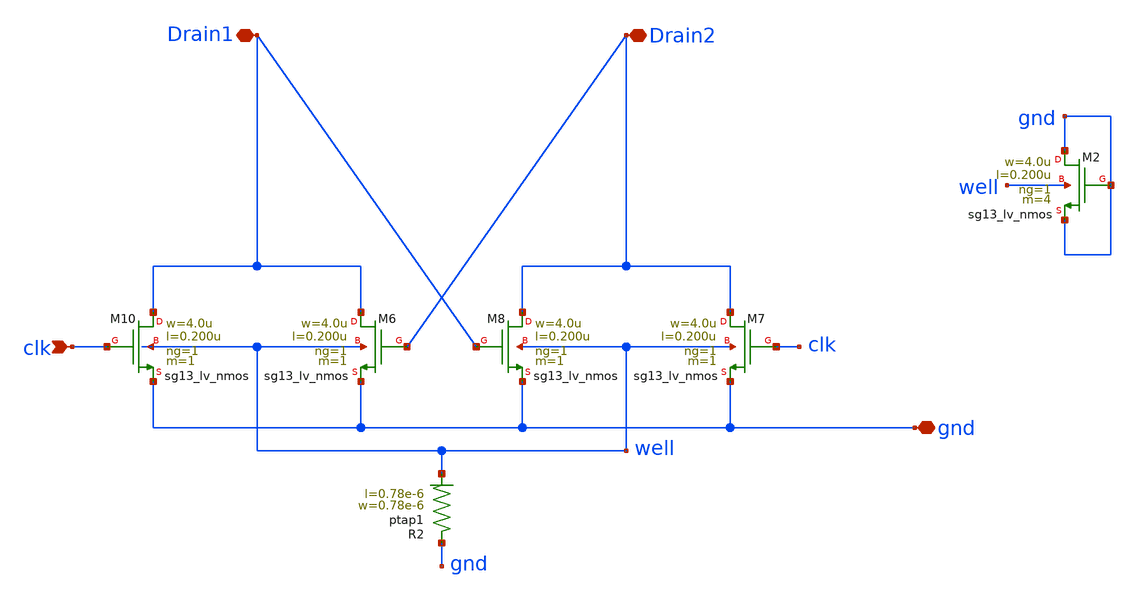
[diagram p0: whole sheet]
** sch_path: modules/module_3_8_bit_SAR_ADC/part_5_analog_layout/comparator/layout/misc/load/schematic_mod/load.sch
**.subckt load gnd clk Drain1 Drain2
*.iopin gnd
*.ipin clk
*.iopin Drain1
*.iopin Drain2
XM6 Drain1 Drain2 gnd well sg13_lv_nmos w=4.0u l=0.200u ng=1 m=1 mm_ok=1
XM10 Drain1 clk gnd well sg13_lv_nmos w=4.0u l=0.200u ng=1 m=1 mm_ok=1
XM7 Drain2 clk gnd well sg13_lv_nmos w=4.0u l=0.200u ng=1 m=1 mm_ok=1
XM8 Drain2 Drain1 gnd well sg13_lv_nmos w=4.0u l=0.200u ng=1 m=1 mm_ok=1
XR2 gnd well ptap1 R=262.8 w=0.78e-6 l=0.78e-6
XM2 gnd gnd gnd well sg13_lv_nmos w=4.0u l=0.200u ng=1 m=4 mm_ok=1
**.ends
.end
